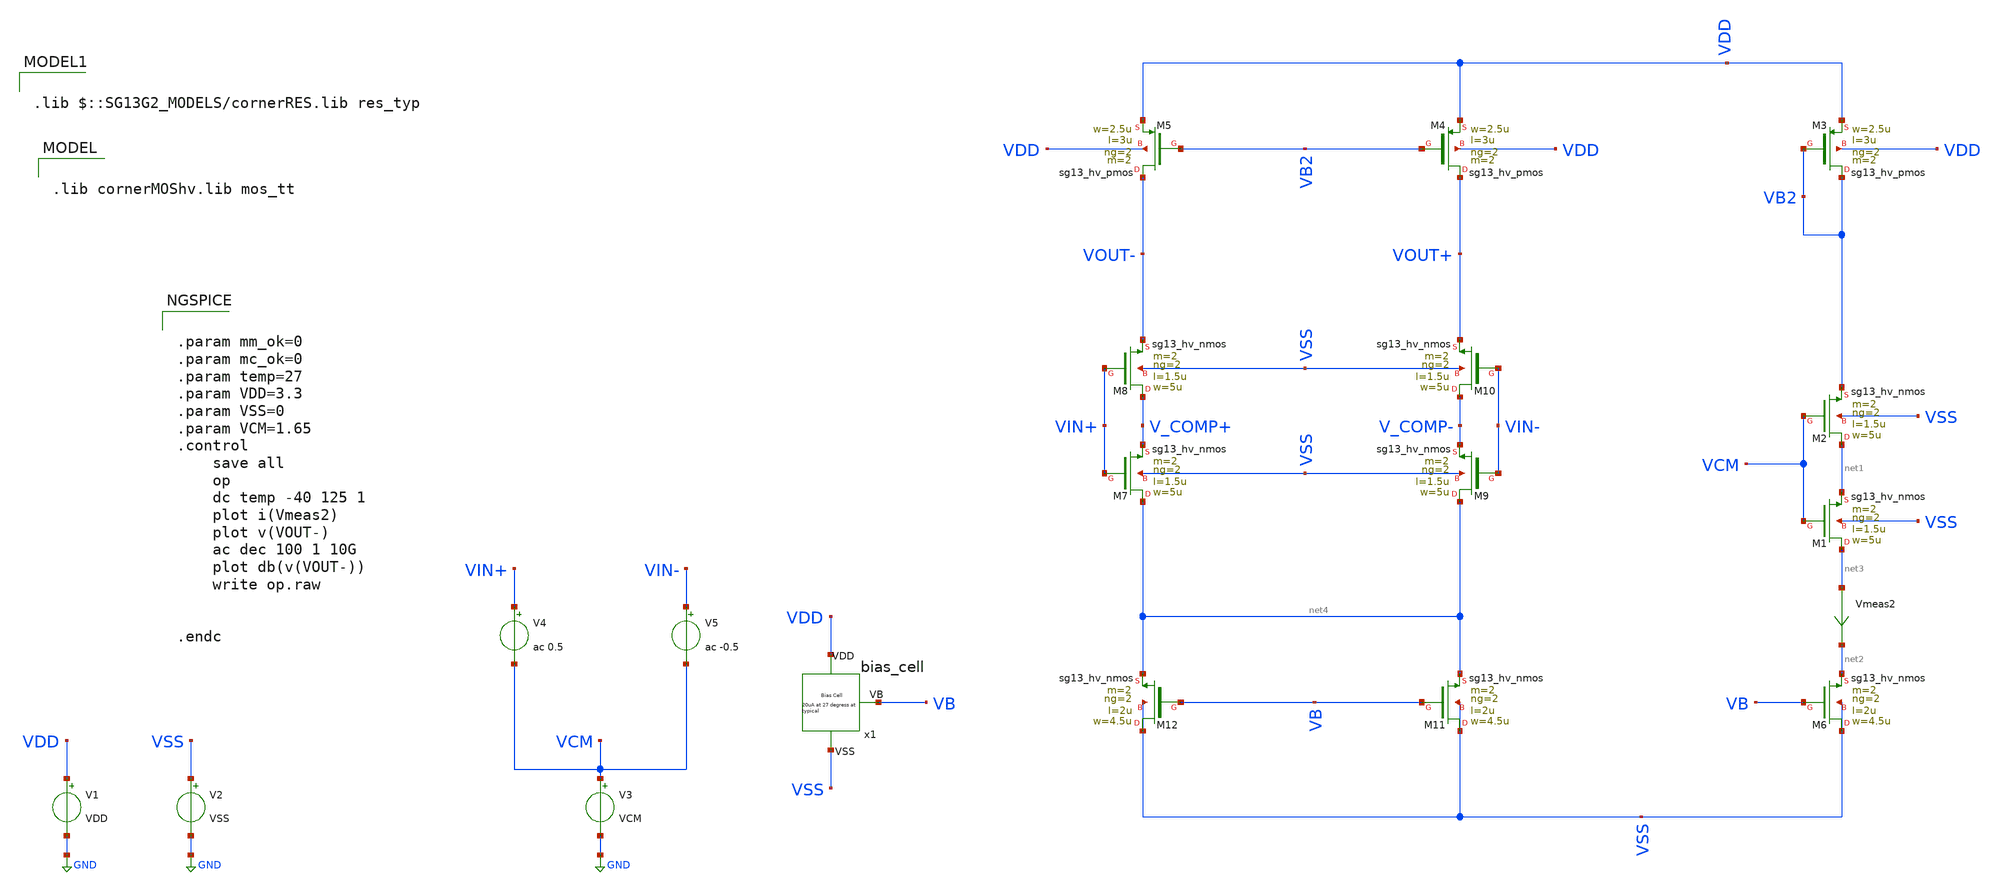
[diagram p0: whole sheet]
** sch_path: Learning/fully_differencial/Indirect_Compensation_Techniques_for_Three_Stage_Fully_Differential_Op_amps_IHP130/testbenches/first_stage_sim.sch
**.subckt first_stage_sim
x1 VDD VSS VB bias_cell
V1 VDD GND VDD
V2 VSS GND VSS
XM6 VSS VB net2 VSS sg13_hv_nmos w=4.5u l=2u ng=2 m=2 mm_ok=1
XM1 net3 VCM net1 VSS sg13_hv_nmos w=5u l=1.5u ng=2 m=2 mm_ok=1
XM2 net1 VCM VB2 VSS sg13_hv_nmos w=5u l=1.5u ng=2 m=2 mm_ok=1
V3 VCM GND VCM
XM3 VB2 VB2 VDD VDD sg13_hv_pmos w=2.5u l=3u ng=2 m=2 mm_ok=1
Vmeas2 net3 net2 0
.save i(vmeas2)
XM7 net4 VIN+ V_COMP+ VSS sg13_hv_nmos w=5u l=1.5u ng=2 m=2 mm_ok=1
XM8 V_COMP+ VIN+ VOUT- VSS sg13_hv_nmos w=5u l=1.5u ng=2 m=2 mm_ok=1
XM9 net4 VIN- V_COMP- VSS sg13_hv_nmos w=5u l=1.5u ng=2 m=2 mm_ok=1
XM10 V_COMP- VIN- VOUT+ VSS sg13_hv_nmos w=5u l=1.5u ng=2 m=2 mm_ok=1
XM11 VSS VB net4 VSS sg13_hv_nmos w=4.5u l=2u ng=2 m=2 mm_ok=1
XM12 VSS VB net4 VSS sg13_hv_nmos w=4.5u l=2u ng=2 m=2 mm_ok=1
V4 VIN+ VCM ac 0.5
V5 VIN- VCM ac -0.5
XM4 VOUT+ VB2 VDD VDD sg13_hv_pmos w=2.5u l=3u ng=2 m=2 mm_ok=1
XM5 VOUT- VB2 VDD VDD sg13_hv_pmos w=2.5u l=3u ng=2 m=2 mm_ok=1
**** begin user architecture code


.param mm_ok=0
.param mc_ok=0
.param temp=27
.param VDD=3.3
.param VSS=0
.param VCM=1.65
.control
	save all
	op
	dc temp -40 125 1
	plot i(Vmeas2)
	plot v(VOUT-)
	ac dec 100 1 10G
	plot db(v(VOUT-))
	write op.raw


.endc



.lib cornerMOShv.lib mos_tt


.lib $::SG13G2_MODELS/cornerRES.lib res_typ

**** end user architecture code
**.ends
.GLOBAL GND
.end
